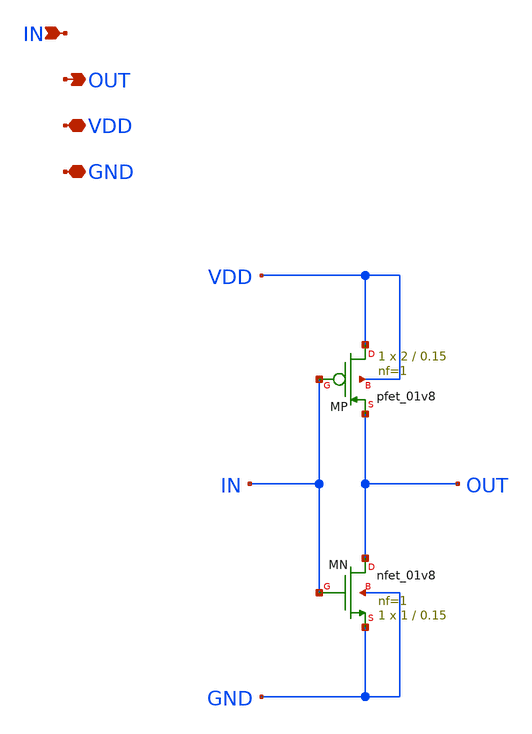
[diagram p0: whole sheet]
** sch_path: blocks/06_Clock_gen/xschem/B6_INV.sch
**.subckt B6_INV IN OUT VDD GND
*.ipin IN
*.opin OUT
*.iopin VDD
*.iopin GND
XMP VDD IN OUT VDD sky130_fd_pr__pfet_01v8 L=0.15 W=2 nf=1 ad='int((1 + 1)/2) * 2 / 1 * 0.29' as='int((1 + 2)/2) * 2 / 1 * 0.29'
+ pd='2*int((1 + 1)/2) * (2 / 1 + 0.29)' ps='2*int((1 + 2)/2) * (2 / 1 + 0.29)' nrd='0.29 / 2 ' nrs='0.29 / 2 '
+ sa=0 sb=0 sd=0 mult=1 m=1
XMN OUT IN GND GND sky130_fd_pr__nfet_01v8 L=0.15 W=1 nf=1 ad='int((1 + 1)/2) * 1 / 1 * 0.29' as='int((1 + 2)/2) * 1 / 1 * 0.29'
+ pd='2*int((1 + 1)/2) * (1 / 1 + 0.29)' ps='2*int((1 + 2)/2) * (1 / 1 + 0.29)' nrd='0.29 / 1 ' nrs='0.29 / 1 '
+ sa=0 sb=0 sd=0 mult=1 m=1
**.ends
.end
